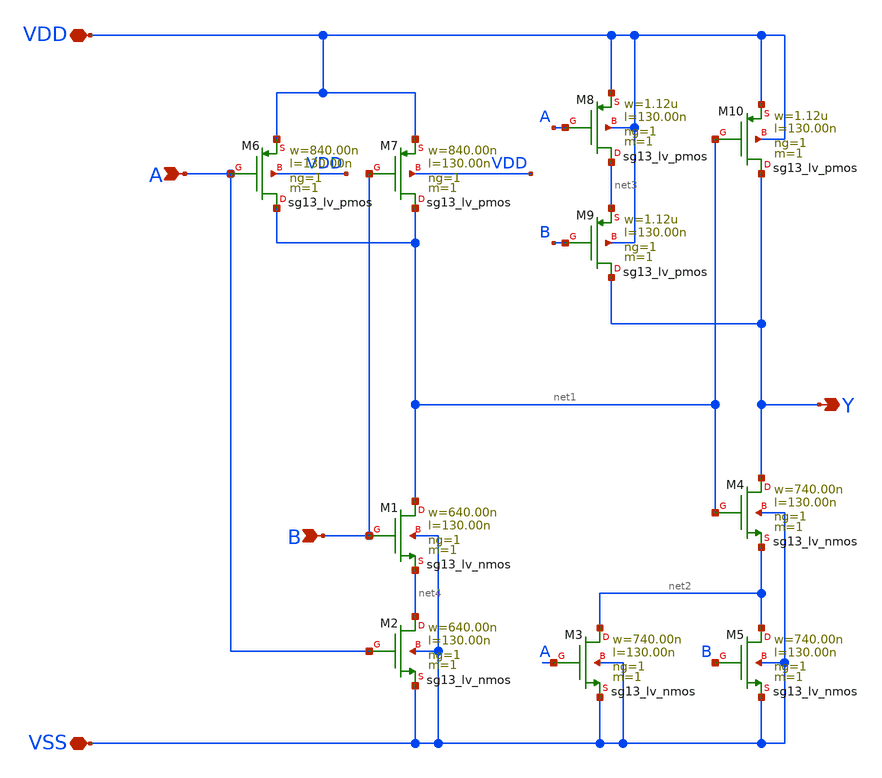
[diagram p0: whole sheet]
** sch_path: ihp-sg13g2/libs.tech/xschem/sg13g2_stdcells/sg13g2_xnor2_1.sch
* Copyright 2023 IHP PDK Authors
* Licensed under the Apache License, Version 2.0 (the "License");
* you may not use this file except in compliance with the License.
* You may obtain a copy of the License at
* https://www.apache.org/licenses/LICENSE-2.0
* Unless required by applicable law or agreed to in writing, software
* distributed under the License is distributed on an "AS IS" BASIS,
* WITHOUT WARRANTIES OR CONDITIONS OF ANY KIND, either express or implied.
* See the License for the specific language governing permissions and
* limitations under the License.
**.subckt sg13g2_xnor2_1 A Y B VDD VSS
*.ipin A
*.opin Y
*.ipin B
*.iopin VDD
*.iopin VSS
XM1 net1 B net4 VSS sg13_lv_nmos w=640.00n l=130.00n ng=1 m=1 mm_ok=1
XM2 net4 A VSS VSS sg13_lv_nmos w=640.00n l=130.00n ng=1 m=1 mm_ok=1
XM3 net2 A VSS VSS sg13_lv_nmos w=740.00n l=130.00n ng=1 m=1 mm_ok=1
XM4 Y net1 net2 VSS sg13_lv_nmos w=740.00n l=130.00n ng=1 m=1 mm_ok=1
XM5 net2 B VSS VSS sg13_lv_nmos w=740.00n l=130.00n ng=1 m=1 mm_ok=1
XM6 net1 A VDD VDD sg13_lv_pmos w=840.00n l=130.00n ng=1 m=1 mm_ok=1
XM7 net1 B VDD VDD sg13_lv_pmos w=840.00n l=130.00n ng=1 m=1 mm_ok=1
XM8 net3 A VDD VDD sg13_lv_pmos w=1.12u l=130.00n ng=1 m=1 mm_ok=1
XM9 Y B net3 VDD sg13_lv_pmos w=1.12u l=130.00n ng=1 m=1 mm_ok=1
XM10 Y net1 VDD VDD sg13_lv_pmos w=1.12u l=130.00n ng=1 m=1 mm_ok=1
**.ends
.end
